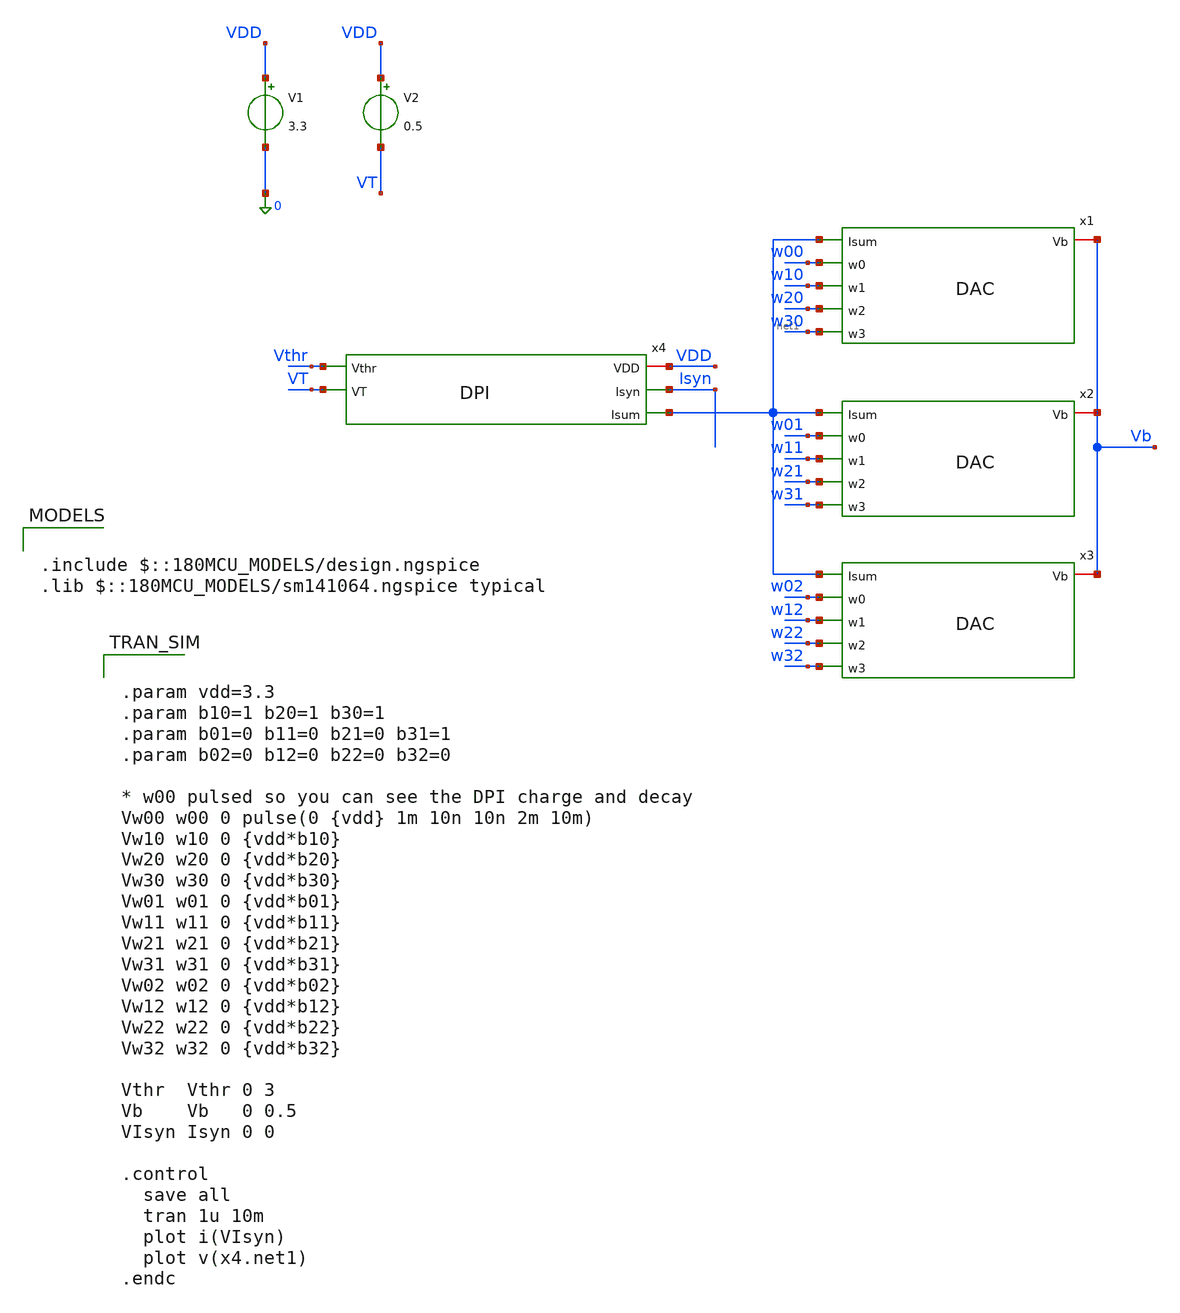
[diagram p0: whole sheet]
** sch_path: analog/neuron/DACs-DPI.sch
**.subckt DACs-DPI
x1 net1 Vb w00 w10 w20 w30 DAC
x2 net1 Vb w01 w11 w21 w31 DAC
x3 net1 Vb w02 w12 w22 w32 DAC
x4 VDD Vthr Isyn net1 VT DPI
V1 VDD 0 3.3
V2 VDD VT 0.5
**** begin user architecture code

.include $::180MCU_MODELS/design.ngspice
.lib $::180MCU_MODELS/sm141064.ngspice typical



.param vdd=3.3
.param b10=1 b20=1 b30=1
.param b01=0 b11=0 b21=0 b31=1
.param b02=0 b12=0 b22=0 b32=0

* w00 pulsed so you can see the DPI charge and decay
Vw00 w00 0 pulse(0 {vdd} 1m 10n 10n 2m 10m)
Vw10 w10 0 {vdd*b10}
Vw20 w20 0 {vdd*b20}
Vw30 w30 0 {vdd*b30}
Vw01 w01 0 {vdd*b01}
Vw11 w11 0 {vdd*b11}
Vw21 w21 0 {vdd*b21}
Vw31 w31 0 {vdd*b31}
Vw02 w02 0 {vdd*b02}
Vw12 w12 0 {vdd*b12}
Vw22 w22 0 {vdd*b22}
Vw32 w32 0 {vdd*b32}

Vthr  Vthr 0 3
Vb    Vb   0 0.5
VIsyn Isyn 0 0

.control
  save all
  tran 1u 10m
  plot i(VIsyn)
  plot v(x4.net1)
.endc



**** end user architecture code
**.ends

* expanding   symbol:  DAC.sym # of pins=6
** sym_path: analog/neuron/DAC.sym
** sch_path: analog/neuron/DAC.sch
.subckt DAC Isum Vb w0 w1 w2 w3
*.iopin Vb
*.ipin w0
*.ipin w1
*.ipin w2
*.ipin w3
*.ipin Isum
XM1 Isum w0 net4 net4 nfet_03v3 L=0.28u W=0.22u nf=1 ad='int((nf+1)/2) * W/nf * 0.18u' as='int((nf+2)/2) * W/nf * 0.18u'
+ pd='2*int((nf+1)/2) * (W/nf + 0.18u)' ps='2*int((nf+2)/2) * (W/nf + 0.18u)' nrd='0.18u / W' nrs='0.18u / W'
+ sa=0 sb=0 sd=0 m=1
XM2 net4 Vb GND GND nfet_03v3 L=0.28u W=0.22u nf=1 ad='int((nf+1)/2) * W/nf * 0.18u' as='int((nf+2)/2) * W/nf * 0.18u'
+ pd='2*int((nf+1)/2) * (W/nf + 0.18u)' ps='2*int((nf+2)/2) * (W/nf + 0.18u)' nrd='0.18u / W' nrs='0.18u / W'
+ sa=0 sb=0 sd=0 m=1
XM3 Isum w1 net2 net2 nfet_03v3 L=0.28u W=0.22u nf=1 ad='int((nf+1)/2) * W/nf * 0.18u' as='int((nf+2)/2) * W/nf * 0.18u'
+ pd='2*int((nf+1)/2) * (W/nf + 0.18u)' ps='2*int((nf+2)/2) * (W/nf + 0.18u)' nrd='0.18u / W' nrs='0.18u / W'
+ sa=0 sb=0 sd=0 m=1
XM4 net2 Vb GND GND nfet_03v3 L=0.28u W=0.22u nf=1 ad='int((nf+1)/2) * W/nf * 0.18u' as='int((nf+2)/2) * W/nf * 0.18u'
+ pd='2*int((nf+1)/2) * (W/nf + 0.18u)' ps='2*int((nf+2)/2) * (W/nf + 0.18u)' nrd='0.18u / W' nrs='0.18u / W'
+ sa=0 sb=0 sd=0 m=1
XM5 Isum w2 net3 net3 nfet_03v3 L=0.28u W=0.22u nf=1 ad='int((nf+1)/2) * W/nf * 0.18u' as='int((nf+2)/2) * W/nf * 0.18u'
+ pd='2*int((nf+1)/2) * (W/nf + 0.18u)' ps='2*int((nf+2)/2) * (W/nf + 0.18u)' nrd='0.18u / W' nrs='0.18u / W'
+ sa=0 sb=0 sd=0 m=1
XM6 net3 Vb GND GND nfet_03v3 L=0.28u W=0.22u nf=1 ad='int((nf+1)/2) * W/nf * 0.18u' as='int((nf+2)/2) * W/nf * 0.18u'
+ pd='2*int((nf+1)/2) * (W/nf + 0.18u)' ps='2*int((nf+2)/2) * (W/nf + 0.18u)' nrd='0.18u / W' nrs='0.18u / W'
+ sa=0 sb=0 sd=0 m=1
XM7 Isum w3 net1 net1 nfet_03v3 L=0.28u W=0.22u nf=1 ad='int((nf+1)/2) * W/nf * 0.18u' as='int((nf+2)/2) * W/nf * 0.18u'
+ pd='2*int((nf+1)/2) * (W/nf + 0.18u)' ps='2*int((nf+2)/2) * (W/nf + 0.18u)' nrd='0.18u / W' nrs='0.18u / W'
+ sa=0 sb=0 sd=0 m=1
XM8 net1 Vb GND GND nfet_03v3 L=0.28u W=0.22u nf=1 ad='int((nf+1)/2) * W/nf * 0.18u' as='int((nf+2)/2) * W/nf * 0.18u'
+ pd='2*int((nf+1)/2) * (W/nf + 0.18u)' ps='2*int((nf+2)/2) * (W/nf + 0.18u)' nrd='0.18u / W' nrs='0.18u / W'
+ sa=0 sb=0 sd=0 m=1
.ends


* expanding   symbol:  DPI.sym # of pins=5
** sym_path: analog/neuron/DPI.sym
** sch_path: analog/neuron/DPI.sch
.subckt DPI VDD Vthr Isyn Isum VT
*.ipin Vthr
*.iopin VDD
*.opin Isyn
*.opin Isum
*.ipin VT
XM1 VDD Vthr Isum Isum nfet_03v3 L=0.28u W=0.22u nf=1 ad='int((nf+1)/2) * W/nf * 0.18u' as='int((nf+2)/2) * W/nf * 0.18u'
+ pd='2*int((nf+1)/2) * (W/nf + 0.18u)' ps='2*int((nf+2)/2) * (W/nf + 0.18u)' nrd='0.18u / W' nrs='0.18u / W'
+ sa=0 sb=0 sd=0 m=1
XM2 net1 net1 Isum Isum nfet_03v3 L=0.28u W=0.22u nf=1 ad='int((nf+1)/2) * W/nf * 0.18u' as='int((nf+2)/2) * W/nf * 0.18u'
+ pd='2*int((nf+1)/2) * (W/nf + 0.18u)' ps='2*int((nf+2)/2) * (W/nf + 0.18u)' nrd='0.18u / W' nrs='0.18u / W'
+ sa=0 sb=0 sd=0 m=1
XM3 net1 VT VDD VDD pfet_03v3 L=0.28u W=0.22u nf=1 ad='int((nf+1)/2) * W/nf * 0.18u' as='int((nf+2)/2) * W/nf * 0.18u'
+ pd='2*int((nf+1)/2) * (W/nf + 0.18u)' ps='2*int((nf+2)/2) * (W/nf + 0.18u)' nrd='0.18u / W' nrs='0.18u / W'
+ sa=0 sb=0 sd=0 m=1
XM4 Isyn net1 VDD VDD pfet_03v3 L=0.28u W=0.22u nf=1 ad='int((nf+1)/2) * W/nf * 0.18u' as='int((nf+2)/2) * W/nf * 0.18u'
+ pd='2*int((nf+1)/2) * (W/nf + 0.18u)' ps='2*int((nf+2)/2) * (W/nf + 0.18u)' nrd='0.18u / W' nrs='0.18u / W'
+ sa=0 sb=0 sd=0 m=1
C4 VDD net1 1p m=1
.ends

.GLOBAL GND
.end
